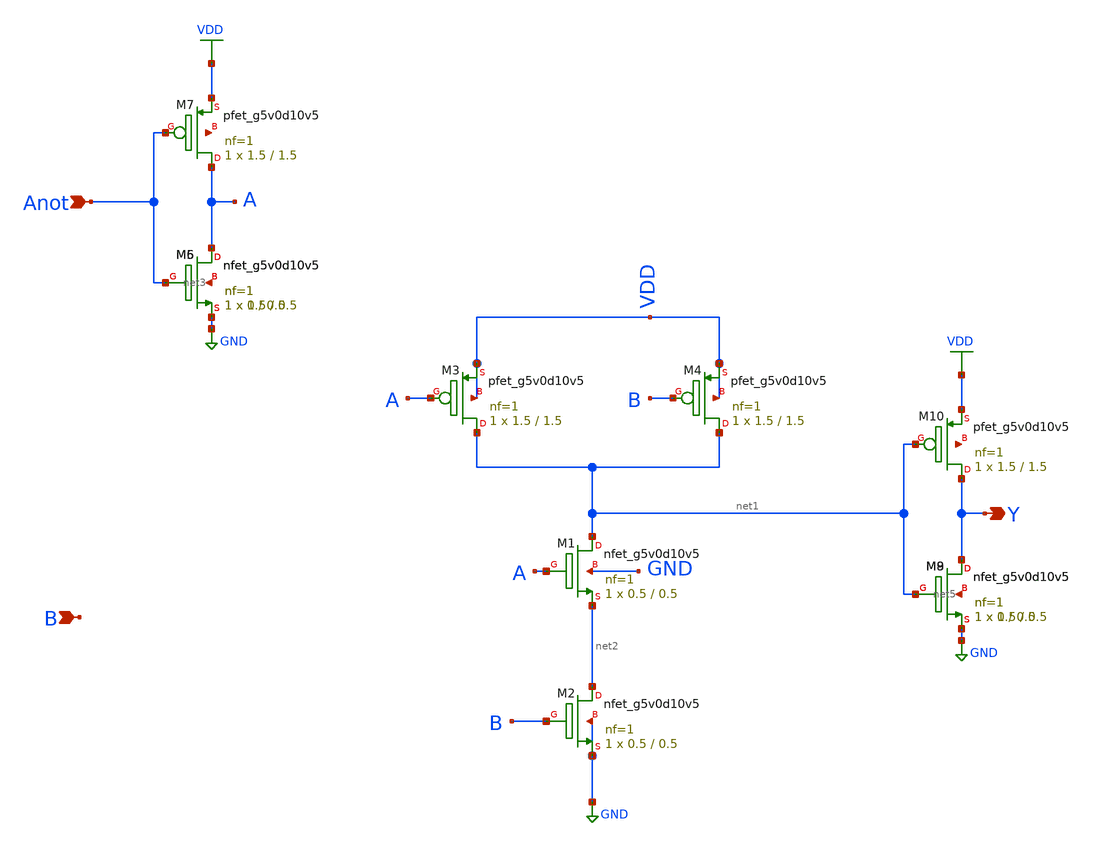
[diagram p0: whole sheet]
** sch_path: xschem/StandardCells/2_1NAND.sch
**.subckt 2_1NAND Anot B Y
*.ipin Anot
*.ipin B
*.opin Y
XM1 net1 A net2 GND sky130_fd_pr__nfet_g5v0d10v5 L=0.5 W=0.5 nf=1 ad='int((nf+1)/2) * W/nf * 0.29' as='int((nf+2)/2) * W/nf * 0.29'
+ pd='2*int((nf+1)/2) * (W/nf + 0.29)' ps='2*int((nf+2)/2) * (W/nf + 0.29)' nrd='0.29 / W' nrs='0.29 / W'
+ sa=0 sb=0 sd=0 mult=1 m=1
XM2 net2 B GND GND sky130_fd_pr__nfet_g5v0d10v5 L=0.5 W=0.5 nf=1 ad='int((nf+1)/2) * W/nf * 0.29' as='int((nf+2)/2) * W/nf * 0.29'
+ pd='2*int((nf+1)/2) * (W/nf + 0.29)' ps='2*int((nf+2)/2) * (W/nf + 0.29)' nrd='0.29 / W' nrs='0.29 / W'
+ sa=0 sb=0 sd=0 mult=1 m=1
XM3 net1 A VDD VDD sky130_fd_pr__pfet_g5v0d10v5 L=1.5 W=1.5 nf=1 ad='int((nf+1)/2) * W/nf * 0.29' as='int((nf+2)/2) * W/nf * 0.29'
+ pd='2*int((nf+1)/2) * (W/nf + 0.29)' ps='2*int((nf+2)/2) * (W/nf + 0.29)' nrd='0.29 / W' nrs='0.29 / W'
+ sa=0 sb=0 sd=0 mult=1 m=1
XM4 net1 B VDD VDD sky130_fd_pr__pfet_g5v0d10v5 L=1.5 W=1.5 nf=1 ad='int((nf+1)/2) * W/nf * 0.29' as='int((nf+2)/2) * W/nf * 0.29'
+ pd='2*int((nf+1)/2) * (W/nf + 0.29)' ps='2*int((nf+2)/2) * (W/nf + 0.29)' nrd='0.29 / W' nrs='0.29 / W'
+ sa=0 sb=0 sd=0 mult=1 m=1
XM5 A Anot GND net3 sky130_fd_pr__nfet_g5v0d10v5 L=0.5 W=0.5 nf=1 ad='int((nf+1)/2) * W/nf * 0.29' as='int((nf+2)/2) * W/nf * 0.29'
+ pd='2*int((nf+1)/2) * (W/nf + 0.29)' ps='2*int((nf+2)/2) * (W/nf + 0.29)' nrd='0.29 / W' nrs='0.29 / W'
+ sa=0 sb=0 sd=0 mult=1 m=1
XM6 A Anot GND net3 sky130_fd_pr__nfet_g5v0d10v5 L=0.5 W=1 nf=1 ad='int((nf+1)/2) * W/nf * 0.29' as='int((nf+2)/2) * W/nf * 0.29'
+ pd='2*int((nf+1)/2) * (W/nf + 0.29)' ps='2*int((nf+2)/2) * (W/nf + 0.29)' nrd='0.29 / W' nrs='0.29 / W'
+ sa=0 sb=0 sd=0 mult=1 m=1
XM7 A Anot VDD net4 sky130_fd_pr__pfet_g5v0d10v5 L=1.5 W=1.5 nf=1 ad='int((nf+1)/2) * W/nf * 0.29' as='int((nf+2)/2) * W/nf * 0.29'
+ pd='2*int((nf+1)/2) * (W/nf + 0.29)' ps='2*int((nf+2)/2) * (W/nf + 0.29)' nrd='0.29 / W' nrs='0.29 / W'
+ sa=0 sb=0 sd=0 mult=1 m=1
XM8 Y net1 GND net5 sky130_fd_pr__nfet_g5v0d10v5 L=0.5 W=0.5 nf=1 ad='int((nf+1)/2) * W/nf * 0.29' as='int((nf+2)/2) * W/nf * 0.29'
+ pd='2*int((nf+1)/2) * (W/nf + 0.29)' ps='2*int((nf+2)/2) * (W/nf + 0.29)' nrd='0.29 / W' nrs='0.29 / W'
+ sa=0 sb=0 sd=0 mult=1 m=1
XM9 Y net1 GND net5 sky130_fd_pr__nfet_g5v0d10v5 L=0.5 W=1 nf=1 ad='int((nf+1)/2) * W/nf * 0.29' as='int((nf+2)/2) * W/nf * 0.29'
+ pd='2*int((nf+1)/2) * (W/nf + 0.29)' ps='2*int((nf+2)/2) * (W/nf + 0.29)' nrd='0.29 / W' nrs='0.29 / W'
+ sa=0 sb=0 sd=0 mult=1 m=1
XM10 Y net1 VDD net6 sky130_fd_pr__pfet_g5v0d10v5 L=1.5 W=1.5 nf=1 ad='int((nf+1)/2) * W/nf * 0.29' as='int((nf+2)/2) * W/nf * 0.29'
+ pd='2*int((nf+1)/2) * (W/nf + 0.29)' ps='2*int((nf+2)/2) * (W/nf + 0.29)' nrd='0.29 / W' nrs='0.29 / W'
+ sa=0 sb=0 sd=0 mult=1 m=1
**.ends
.GLOBAL VDD
.GLOBAL GND
.end
